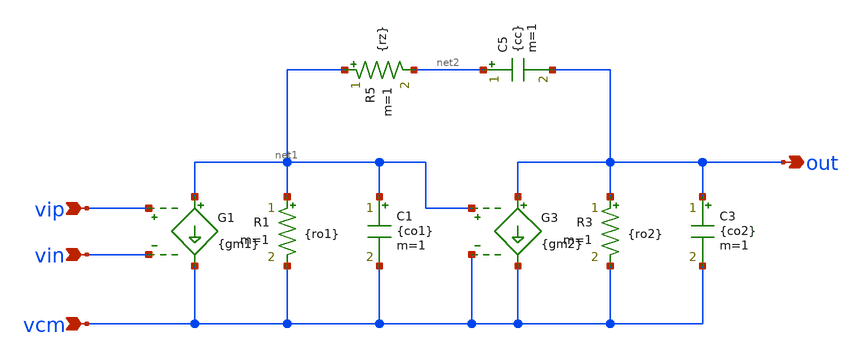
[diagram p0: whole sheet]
** sch_path: modules/ideal_op_single_2stage.sch
**.subckt ideal_op_single_2stage vip vin out vcm
*.ipin vip
*.ipin vin
*.opin out
*.ipin vcm
G1 net1 vcm vip vin {gm1}
R1 net1 vcm {ro1} m=1
C1 net1 vcm {co1} m=1
G3 out vcm net1 vcm {gm2}
R3 out vcm {ro2} m=1
C3 out vcm {co2} m=1
R5 net1 net2 {rz} m=1
C5 net2 out {cc} m=1
**.ends
.end
